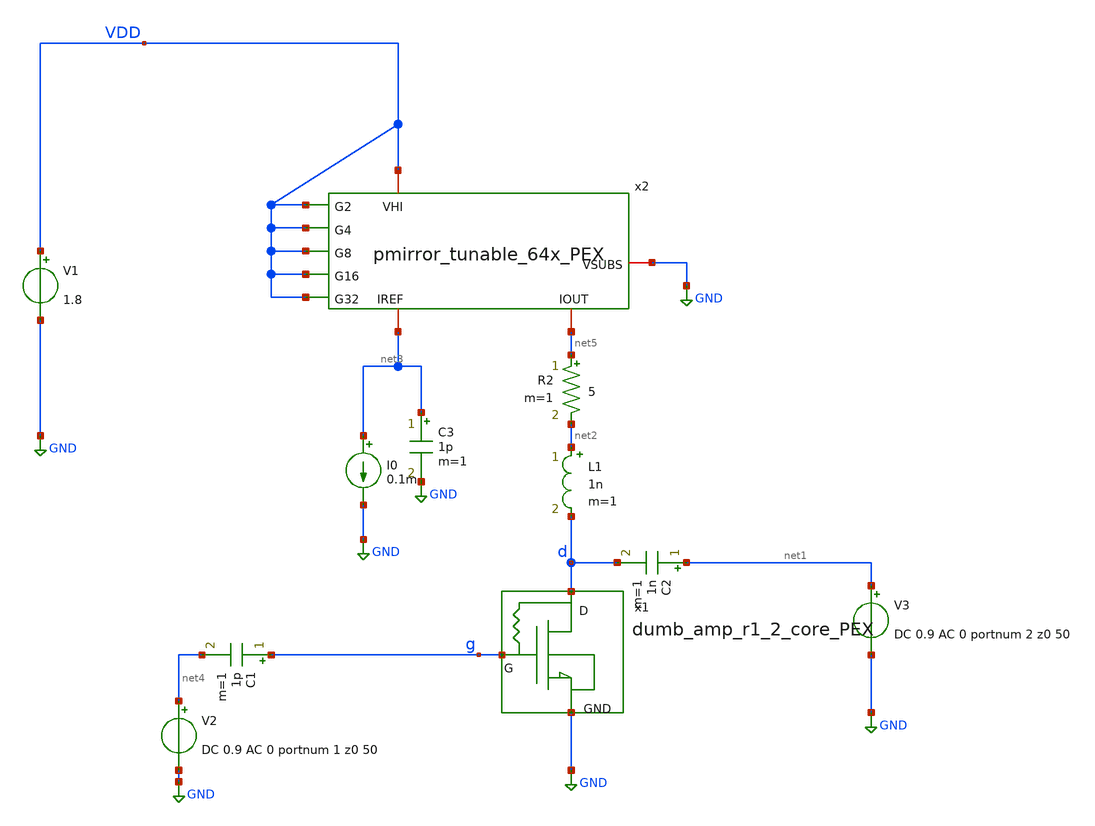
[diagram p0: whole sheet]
** sch_path: xschem/dumb_amp_r1_2_PEX.sch
**.subckt dumb_amp_r1_2_PEX
V1 VDD GND 1.8
V3 net1 GND DC 0.9 AC 0 portnum 2 z0 50
V2 net4 GND DC 0.9 AC 0 portnum 1 z0 50
C1 g net4 1p m=1
C2 net1 d 1n m=1
L1 net2 d 1n m=1
R2 net5 net2 5 m=1
I0 net3 GND 0.1m
C3 net3 GND 1p m=1
x1 g d GND dumb_amp_r1_2_core_PEX
x2 VDD VDD VDD GND VDD net3 net5 VDD VDD pmirror_tunable_64x_PEX
**** begin user architecture code
.lib $::SKYWATER_MODELS/sky130.lib.spice tt
* .include $::PDKPATH/libs.ref/sky130_fd_sc_hvl/spice/sky130_fd_sc_hvl.spice


.subckt DUT NGATE NDRAIN VSUBS
.subckt sky130_fd_pr__rf_nfet_01v8_aM02W5p00L0p15 DRAIN GATE SOURCE SUBSTRATE
X0 DRAIN GATE SOURCE SUBSTRATE sky130_fd_pr__nfet_01v8 ad=1.414e+12p pd=1.066e+07u as=2.828e+12p
+ ps=2.132e+07u w=5.05e+06u l=150000u
X1 SOURCE GATE DRAIN SUBSTRATE sky130_fd_pr__nfet_01v8 ad=0p pd=0u as=0p ps=0u w=5.05e+06u l=150000u
C0 DRAIN SOURCE 3.59fF
C1 GATE SOURCE 0.46fF
C2 DRAIN GATE 0.34fF
C3 DRAIN SUBSTRATE 0.40fF
C4 SOURCE SUBSTRATE 2.44fF
C5 GATE SUBSTRATE 0.64fF
.ends

.subckt nfet_3x_2 D G S sub
Xsky130_fd_pr__rf_nfet_01v8_aM02W5p00L0p15_0 D G S sub sky130_fd_pr__rf_nfet_01v8_aM02W5p00L0p15
Xsky130_fd_pr__rf_nfet_01v8_aM02W5p00L0p15_1 D G S sub sky130_fd_pr__rf_nfet_01v8_aM02W5p00L0p15
Xsky130_fd_pr__rf_nfet_01v8_aM02W5p00L0p15_2 D G S sub sky130_fd_pr__rf_nfet_01v8_aM02W5p00L0p15
C0 G sub 1.34fF
C1 S D -0.11fF
C2 S G 2.13fF
C3 G D 1.69fF
C4 S sub -0.01fF
C5 D sub -0.05fF
C6 sub 0 -1.34fF
C7 D 0 0.62fF
C8 S 0 6.66fF
C9 G 0 1.96fF
.ends

.subckt RF_nfet_6xaM02W5p0L0p15 G S D B
Xnfet_3x_2_0 D G S B nfet_3x_2
Xnfet_3x_2_1 D G S B nfet_3x_2
C0 D B -0.02fF
C1 G S 0.20fF
C2 G B 0.06fF
C3 G D 0.14fF
C4 S B 0.02fF
C5 D S 0.01fF
C6 B 0 -3.73fF
C7 D 0 1.02fF
C8 S 0 13.03fF
C9 G 0 3.30fF
.ends


.subckt sky130_fd_pr__res_generic_po_JFYRVD a_75_284# a_n141_n357# a_n271_n487#
R0 a_n141_n357# a_75_284# sky130_fd_pr__res_generic_po w=330000u l=6.2e+06u
C0 a_n141_n357# a_n271_n487# 0.14fF
C1 a_75_284# a_n271_n487# 0.14fF
.ends

XRF_nfet_6xaM02W5p0L0p15_0 NGATE NDRAIN VSUBS VSUBS RF_nfet_6xaM02W5p0L0p15
Xsky130_fd_pr__res_generic_po_JFYRVD_0 NGATE NDRAIN VSUBS sky130_fd_pr__res_generic_po_JFYRVD
C0 VSUBS NDRAIN 1.42fF
C1 NGATE VSUBS 2.81fF
C2 NGATE NDRAIN 2.91fF
C5 NDRAIN VSUBS 14.22fF
C6 NGATE VSUBS 3.28fF
.ends

XDUT G D GND DUT




.sp dec 1000 1e9 10e9 1


* .ac dec 1000 0.01e9 100e9
.control
run
display

let z11=50*(1+s_1_1)/(1-s_1_1)
let z22=50*(1+s_2_2)/(1-s_2_2)
let S11 = S_1_1
let S21 = S_2_1
let S12 = S_1_2
let S22 = S_2_2

* Stability
let delta=S11*S22-S12*S21
let K    = (1-mag(S11)^2-mag(S22)^2+mag(delta)^2)/(2*mag(S12*S21))
let mu   = (1-mag(S11)^2)/(mag(S22-conj(S11)*delta)+mag(S21*S12))
* plot real(z11) real(z22)
* plot imag(z11) imag(z22)
plot db(S_1_1) db(S_2_2) db(S_2_1)
*
plot db(K)
plot mag(delta)
plot db(mu)
plot NF NFmin
.endc


**** end user architecture code
**.ends

* expanding   symbol:  dumb_amp_r1_2_core_PEX.sym # of pins=3
** sym_path: xschem/dumb_amp_r1_2_core_PEX.sym
** sch_path: xschem/dumb_amp_r1_2_core_PEX.sch
.subckt dumb_amp_r1_2_core_PEX G D GND
*.iopin G
*.iopin D
*.iopin GND
**** begin user architecture code

.subckt dumb_amp_core_pex NGATE NDRAIN VSUBS
.subckt sky130_fd_pr__rf_nfet_01v8_aM02W5p00L0p15 DRAIN GATE SOURCE SUBSTRATE
X0 DRAIN GATE SOURCE SUBSTRATE sky130_fd_pr__nfet_01v8 ad=1.414e+12p pd=1.066e+07u as=2.828e+12p
+ ps=2.132e+07u w=5.05e+06u l=150000u
X1 SOURCE GATE DRAIN SUBSTRATE sky130_fd_pr__nfet_01v8 ad=0p pd=0u as=0p ps=0u w=5.05e+06u l=150000u
C0 DRAIN SOURCE 3.59fF
C1 GATE SOURCE 0.46fF
C2 DRAIN GATE 0.34fF
C3 DRAIN SUBSTRATE 0.40fF
C4 SOURCE SUBSTRATE 2.44fF
C5 GATE SUBSTRATE 0.64fF
.ends
.subckt nfet_3x_2 D G S sub
Xsky130_fd_pr__rf_nfet_01v8_aM02W5p00L0p15_0 D G S sub sky130_fd_pr__rf_nfet_01v8_aM02W5p00L0p15
Xsky130_fd_pr__rf_nfet_01v8_aM02W5p00L0p15_1 D G S sub sky130_fd_pr__rf_nfet_01v8_aM02W5p00L0p15
Xsky130_fd_pr__rf_nfet_01v8_aM02W5p00L0p15_2 D G S sub sky130_fd_pr__rf_nfet_01v8_aM02W5p00L0p15
C0 G sub 1.34fF
C1 S D -0.11fF
C2 S G 2.13fF
C3 G D 1.69fF
C4 S sub -0.01fF
C5 D sub -0.05fF
C6 sub 0 -1.34fF
C7 D 0 0.62fF
C8 S 0 6.66fF
C9 G 0 1.96fF
.ends
.subckt RF_nfet_6xaM02W5p0L0p15 G S D B
Xnfet_3x_2_0 D G S B nfet_3x_2
Xnfet_3x_2_1 D G S B nfet_3x_2
C0 D B -0.02fF
C1 G S 0.20fF
C2 G B 0.06fF
C3 G D 0.14fF
C4 S B 0.02fF
C5 D S 0.01fF
C6 B 0 -3.73fF
C7 D 0 1.02fF
C8 S 0 13.03fF
C9 G 0 3.30fF
.ends
.subckt sky130_fd_pr__res_generic_po_JFYRVD a_75_284# a_n141_n357# a_n271_n487#
R0 a_n141_n357# a_75_284# sky130_fd_pr__res_generic_po w=330000u l=6.2e+06u
C0 a_n141_n357# a_n271_n487# 0.14fF
C1 a_75_284# a_n271_n487# 0.14fF
.ends
XRF_nfet_6xaM02W5p0L0p15_0 NGATE NDRAIN VSUBS VSUBS RF_nfet_6xaM02W5p0L0p15
Xsky130_fd_pr__res_generic_po_JFYRVD_0 NGATE NDRAIN VSUBS sky130_fd_pr__res_generic_po_JFYRVD
C0 VSUBS NDRAIN 1.42fF
C1 NGATE VSUBS 2.81fF
C2 NGATE NDRAIN 2.91fF
C5 NDRAIN VSUBS 14.22fF
C6 NGATE VSUBS 3.28fF
.ends

XDUT G D GND dumb_amp_core_pex


**** end user architecture code
.ends


* expanding   symbol:  pmirror_tunable_64x_PEX.sym # of pins=9
** sym_path: xschem/pmirror_tunable_64x_PEX.sym
** sch_path: xschem/pmirror_tunable_64x_PEX.sch
.subckt pmirror_tunable_64x_PEX VHI G2 G4 VSUBS G8 IREF IOUT G16 G32
*.ipin G2
*.ipin G4
*.ipin G8
*.ipin G16
*.ipin G32
*.iopin VHI
*.iopin VSUBS
*.iopin IREF
*.iopin IOUT
**** begin user architecture code

* SPICE3 file created from pmirror_pfet_64x_complete.ext - technology: sky130B
X0 pmirror_pfet_64x_flat_0/G32 IREF VSUBS sky130_fd_pr__res_xhigh_po_0p35 l=500000u
X1 pmirror_pfet_64x_flat_0/G4  IREF VSUBS sky130_fd_pr__res_xhigh_po_0p35 l=500000u
X2 pmirror_pfet_64x_flat_0/G8  IREF VSUBS sky130_fd_pr__res_xhigh_po_0p35 l=500000u
X3 pmirror_pfet_64x_flat_0/G2  IREF VSUBS sky130_fd_pr__res_xhigh_po_0p35 l=500000u
X5 pmirror_pfet_64x_flat_0/G16 IREF VSUBS sky130_fd_pr__res_xhigh_po_0p35 l=500000u

X7 VHI pmirror_pfet_64x_flat_0/G32 IOUT VHI sky130_fd_pr__pfet_01v8 ad=0p pd=0u as=0p ps=0u w=1e+06u
+ l=300000u
X8 IOUT pmirror_pfet_64x_flat_0/G32 VHI VHI sky130_fd_pr__pfet_01v8 ad=0p pd=0u as=0p ps=0u w=1e+06u
+ l=300000u
X11 IOUT pmirror_pfet_64x_flat_0/G32 VHI VHI sky130_fd_pr__pfet_01v8 ad=0p pd=0u as=0p ps=0u
+ w=1e+06u l=300000u
X16 VHI pmirror_pfet_64x_flat_0/G32 IOUT VHI sky130_fd_pr__pfet_01v8 ad=0p pd=0u as=0p ps=0u
+ w=1e+06u l=300000u
X17 VHI pmirror_pfet_64x_flat_0/G32 IOUT VHI sky130_fd_pr__pfet_01v8 ad=0p pd=0u as=0p ps=0u
+ w=1e+06u l=300000u
X18 VHI pmirror_pfet_64x_flat_0/G32 IOUT VHI sky130_fd_pr__pfet_01v8 ad=0p pd=0u as=0p ps=0u
+ w=1e+06u l=300000u
X21 IOUT pmirror_pfet_64x_flat_0/G32 VHI VHI sky130_fd_pr__pfet_01v8 ad=0p pd=0u as=0p ps=0u
+ w=1e+06u l=300000u
X22 IOUT pmirror_pfet_64x_flat_0/G32 VHI VHI sky130_fd_pr__pfet_01v8 ad=0p pd=0u as=0p ps=0u
+ w=1e+06u l=300000u
X27 IOUT pmirror_pfet_64x_flat_0/G32 VHI VHI sky130_fd_pr__pfet_01v8 ad=1p pd=0u as=0p ps=0u
+ w=1e+06u l=300000u
X28 IOUT pmirror_pfet_64x_flat_0/G32 VHI VHI sky130_fd_pr__pfet_01v8 ad=0p pd=0u as=0p ps=0u
+ w=1e+06u l=300000u
X29 VHI pmirror_pfet_64x_flat_0/G32 IOUT VHI sky130_fd_pr__pfet_01v8 ad=0p pd=0u as=0p ps=0u
+ w=1e+06u l=300000u
X25 VHI pmirror_pfet_64x_flat_0/G32 IOUT VHI sky130_fd_pr__pfet_01v8 ad=0p pd=0u as=0p ps=0u
+ w=1e+06u l=300000u
X35 VHI pmirror_pfet_64x_flat_0/G32 IOUT VHI sky130_fd_pr__pfet_01v8 ad=0p pd=0u as=0p ps=0u
+ w=1e+06u l=300000u
X38 VHI pmirror_pfet_64x_flat_0/G32 IOUT VHI sky130_fd_pr__pfet_01v8 ad=0p pd=0u as=0p ps=0u
+ w=1e+06u l=300000u
X41 VHI pmirror_pfet_64x_flat_0/G32 IOUT VHI sky130_fd_pr__pfet_01v8 ad=0p pd=0u as=0p ps=0u
+ w=1e+06u l=300000u
X43 IOUT pmirror_pfet_64x_flat_0/G32 VHI VHI sky130_fd_pr__pfet_01v8 ad=0p pd=0u as=0p ps=0u
+ w=1e+06u l=300000u
X44 IOUT pmirror_pfet_64x_flat_0/G32 VHI VHI sky130_fd_pr__pfet_01v8 ad=0p pd=0u as=0p ps=0u
+ w=1e+06u l=300000u
X46 VHI pmirror_pfet_64x_flat_0/G32 IOUT VHI sky130_fd_pr__pfet_01v8 ad=0p pd=0u as=0p ps=0u
+ w=1e+06u l=300000u
X54 VHI pmirror_pfet_64x_flat_0/G32 IOUT VHI sky130_fd_pr__pfet_01v8 ad=0p pd=0u as=0p ps=0u
+ w=1e+06u l=300000u
X55 IOUT pmirror_pfet_64x_flat_0/G32 VHI VHI sky130_fd_pr__pfet_01v8 ad=0p pd=0u as=0p ps=0u
+ w=1e+06u l=300000u
X56 IOUT pmirror_pfet_64x_flat_0/G32 VHI VHI sky130_fd_pr__pfet_01v8 ad=0p pd=0u as=0p ps=0u
+ w=1e+06u l=300000u
X60 IOUT pmirror_pfet_64x_flat_0/G32 VHI VHI sky130_fd_pr__pfet_01v8 ad=0p pd=0u as=0p ps=0u
+ w=1e+06u l=300000u
X61 IOUT pmirror_pfet_64x_flat_0/G32 VHI VHI sky130_fd_pr__pfet_01v8 ad=0p pd=0u as=0p ps=0u
+ w=1e+06u l=300000u
X62 VHI pmirror_pfet_64x_flat_0/G32 IOUT VHI sky130_fd_pr__pfet_01v8 ad=0p pd=0u as=0p ps=0u
+ w=1e+06u l=300000u
X67 IOUT pmirror_pfet_64x_flat_0/G32 VHI VHI sky130_fd_pr__pfet_01v8 ad=0p pd=0u as=0p ps=0u
+ w=1e+06u l=300000u
X68 IOUT pmirror_pfet_64x_flat_0/G32 VHI VHI sky130_fd_pr__pfet_01v8 ad=0p pd=0u as=0p ps=0u
+ w=1e+06u l=300000u
X50 VHI pmirror_pfet_64x_flat_0/G32 IOUT VHI sky130_fd_pr__pfet_01v8 ad=0p pd=0u as=0p ps=0u
+ w=1e+06u l=300000u
X73 VHI pmirror_pfet_64x_flat_0/G32 IOUT VHI sky130_fd_pr__pfet_01v8 ad=0p pd=0u as=0p ps=0u
+ w=1e+06u l=300000u
X74 IOUT pmirror_pfet_64x_flat_0/G32 VHI VHI sky130_fd_pr__pfet_01v8 ad=0p pd=0u as=0p ps=0u
+ w=1e+06u l=300000u
X75 IOUT pmirror_pfet_64x_flat_0/G32 VHI VHI sky130_fd_pr__pfet_01v8 ad=0p pd=0u as=0p ps=0u
+ w=1e+06u l=300000u
X69 VHI pmirror_pfet_64x_flat_0/G32 IOUT VHI sky130_fd_pr__pfet_01v8 ad=0p pd=0u as=0p ps=0u
+ w=1e+06u l=300000u
X81 VHI pmirror_pfet_64x_flat_0/G32 IOUT VHI sky130_fd_pr__pfet_01v8 ad=0p pd=0u as=0p ps=0u
+ w=1e+06u l=300000u

X49 VHI VHI IOUT VHI sky130_fd_pr__pfet_01v8 ad=0p pd=0u as=0p ps=0u w=1e+06u l=300000u
X79 IREF IREF VHI VHI sky130_fd_pr__pfet_01v8 ad=0p pd=0u as=0p ps=0u w=1e+06u l=300000u

X6 IOUT pmirror_pfet_64x_flat_0/G16 VHI VHI sky130_fd_pr__pfet_01v8 ad=0p pd=0u as=0p ps=0u w=1e+06u
+ l=300000u
X9 VHI pmirror_pfet_64x_flat_0/G16 IOUT VHI sky130_fd_pr__pfet_01v8 ad=0p pd=0u as=0p ps=0u w=1e+06u
+ l=300000u
X10 IOUT pmirror_pfet_64x_flat_0/G16 VHI VHI sky130_fd_pr__pfet_01v8 ad=0p pd=0u as=0p ps=0u
+ w=1e+06u l=300000u
X19 IOUT pmirror_pfet_64x_flat_0/G16 VHI VHI sky130_fd_pr__pfet_01v8 ad=0p pd=0u as=0p ps=0u
+ w=1e+06u l=300000u
X20 IOUT pmirror_pfet_64x_flat_0/G16 VHI VHI sky130_fd_pr__pfet_01v8 ad=0p pd=0u as=0p ps=0u
+ w=1e+06u l=300000u
X26 VHI pmirror_pfet_64x_flat_0/G16 IOUT VHI sky130_fd_pr__pfet_01v8 ad=0p pd=0u as=0p ps=0u
+ w=1e+06u l=300000u
X30 IOUT pmirror_pfet_64x_flat_0/G16 VHI VHI sky130_fd_pr__pfet_01v8 ad=0p pd=0u as=0p ps=0u
+ w=1e+06u l=300000u
X33 IOUT pmirror_pfet_64x_flat_0/G16 VHI VHI sky130_fd_pr__pfet_01v8 ad=0p pd=0u as=0p ps=0u
+ w=1e+06u l=300000u
X36 VHI pmirror_pfet_64x_flat_0/G16 IOUT VHI sky130_fd_pr__pfet_01v8 ad=0p pd=0u as=0p ps=0u
+ w=1e+06u l=300000u
X45 VHI pmirror_pfet_64x_flat_0/G16 IOUT VHI sky130_fd_pr__pfet_01v8 ad=0p pd=0u as=0p ps=0u
+ w=1e+06u l=300000u
X53 VHI pmirror_pfet_64x_flat_0/G16 IOUT VHI sky130_fd_pr__pfet_01v8 ad=0p pd=0u as=0p ps=0u
+ w=1e+06u l=300000u
X57 VHI pmirror_pfet_64x_flat_0/G16 IOUT VHI sky130_fd_pr__pfet_01v8 ad=0p pd=0u as=0p ps=0u
+ w=1e+06u l=300000u
X58 VHI pmirror_pfet_64x_flat_0/G16 IOUT VHI sky130_fd_pr__pfet_01v8 ad=0p pd=0u as=0p ps=0u
+ w=1e+06u l=300000u
X65 VHI pmirror_pfet_64x_flat_0/G16 IOUT VHI sky130_fd_pr__pfet_01v8 ad=0p pd=0u as=0p ps=0u
+ w=1e+06u l=300000u
X82 IOUT pmirror_pfet_64x_flat_0/G16 VHI VHI sky130_fd_pr__pfet_01v8 ad=0p pd=0u as=0p ps=0u
+ w=1e+06u l=300000u
X83 IOUT pmirror_pfet_64x_flat_0/G16 VHI VHI sky130_fd_pr__pfet_01v8 ad=0p pd=0u as=0p ps=0u
+ w=1e+06u l=300000u

X14 IOUT pmirror_pfet_64x_flat_0/G8 VHI VHI sky130_fd_pr__pfet_01v8 ad=0p pd=0u as=0p ps=0u w=1e+06u
+ l=300000u
X23 VHI pmirror_pfet_64x_flat_0/G8 IOUT VHI sky130_fd_pr__pfet_01v8 ad=0p pd=0u as=0p ps=0u w=1e+06u
+ l=300000u
X31 VHI pmirror_pfet_64x_flat_0/G8 IOUT VHI sky130_fd_pr__pfet_01v8 ad=0p pd=0u as=0p ps=0u w=1e+06u
+ l=300000u
X32 VHI pmirror_pfet_64x_flat_0/G8 IOUT VHI sky130_fd_pr__pfet_01v8 ad=0p pd=0u as=0p ps=0u w=1e+06u
+ l=300000u
X42 VHI pmirror_pfet_64x_flat_0/G8 IOUT VHI sky130_fd_pr__pfet_01v8 ad=0p pd=0u as=0p ps=0u w=1e+06u
+ l=300000u
X72 IOUT pmirror_pfet_64x_flat_0/G8 VHI VHI sky130_fd_pr__pfet_01v8 ad=0p pd=0u as=0p ps=0u w=1e+06u
+ l=300000u
X80 IOUT pmirror_pfet_64x_flat_0/G8 VHI VHI sky130_fd_pr__pfet_01v8 ad=0p pd=0u as=0p ps=0u w=1e+06u
+ l=300000u
X84 IOUT pmirror_pfet_64x_flat_0/G8 VHI VHI sky130_fd_pr__pfet_01v8 ad=0p pd=0u as=0p ps=0u w=1e+06u
+ l=300000u

X85 IOUT pmirror_pfet_64x_flat_0/G4 VHI VHI sky130_fd_pr__pfet_01v8 ad=0p pd=0u as=0p ps=0u w=1e+06u
+ l=300000u
X39 VHI pmirror_pfet_64x_flat_0/G4 IOUT VHI sky130_fd_pr__pfet_01v8 ad=0p pd=0u as=0p ps=0u w=1e+06u
+ l=300000u
X40 VHI pmirror_pfet_64x_flat_0/G4 IOUT VHI sky130_fd_pr__pfet_01v8 ad=0p pd=0u as=0p ps=0u w=1e+06u
+ l=300000u
X70 IOUT pmirror_pfet_64x_flat_0/G4 VHI VHI sky130_fd_pr__pfet_01v8 ad=0p pd=0u as=0p ps=0u w=1e+06u
+ l=300000u

X48 VHI pmirror_pfet_64x_flat_0/G2 IOUT VHI sky130_fd_pr__pfet_01v8 ad=0p pd=0u as=0p ps=0u w=1e+06u
+ l=300000u
X15 IOUT pmirror_pfet_64x_flat_0/G2 VHI VHI sky130_fd_pr__pfet_01v8 ad=0p pd=0u as=0p ps=0u w=1e+06u
+ l=300000u

X86 VHI G32 pmirror_pfet_64x_flat_0/G32 VHI sky130_fd_pr__pfet_01v8 ad=0p pd=0u as=0p ps=0u
+ w=30e+06u l=150000u
X87 VHI G16 pmirror_pfet_64x_flat_0/G16 VHI sky130_fd_pr__pfet_01v8 ad=0p pd=0u as=0p ps=0u
+ w=30e+06u l=150000u
X88 VHI G2 pmirror_pfet_64x_flat_0/G2 VHI sky130_fd_pr__pfet_01v8 ad=0p pd=0u as=0p ps=0u w=30e+06u
+ l=150000u
X89 VHI G4 pmirror_pfet_64x_flat_0/G4 VHI sky130_fd_pr__pfet_01v8 ad=0p pd=0u as=0p ps=0u w=30e+06u
+ l=150000u
X90 VHI G8 pmirror_pfet_64x_flat_0/G8 VHI sky130_fd_pr__pfet_01v8 ad=0p pd=0u as=0p ps=0u w=30e+06u
+ l=150000u

C0 VHI pmirror_pfet_64x_flat_0/G8 10.15fF
C1 pmirror_pfet_64x_flat_0/G16 IOUT 2.36fF
C2 pmirror_pfet_64x_flat_0/G4 VHI 4.30fF
C3 pmirror_pfet_64x_flat_0/G2 IREF 2.13fF
C4 pmirror_pfet_64x_flat_0/G16 pmirror_pfet_64x_flat_0/G8 4.66fF
C5 pmirror_pfet_64x_flat_0/G4 pmirror_pfet_64x_flat_0/G8 3.24fF
C6 pmirror_pfet_64x_flat_0/G2 VHI 4.48fF
C7 pmirror_pfet_64x_flat_0/G4 pmirror_pfet_64x_flat_0/G2 2.55fF
C8 VHI IREF 4.53fF
C9 VHI pmirror_pfet_64x_flat_0/G32 15.40fF
C10 IOUT pmirror_pfet_64x_flat_0/G32 5.39fF
C11 pmirror_pfet_64x_flat_0/G16 pmirror_pfet_64x_flat_0/G32 3.74fF
C12 VHI IOUT 24.04fF
C13 pmirror_pfet_64x_flat_0/G16 VHI 4.93fF
C14 VHI VSUBS 46.10fF


**** end user architecture code
.ends

.GLOBAL GND
.end
